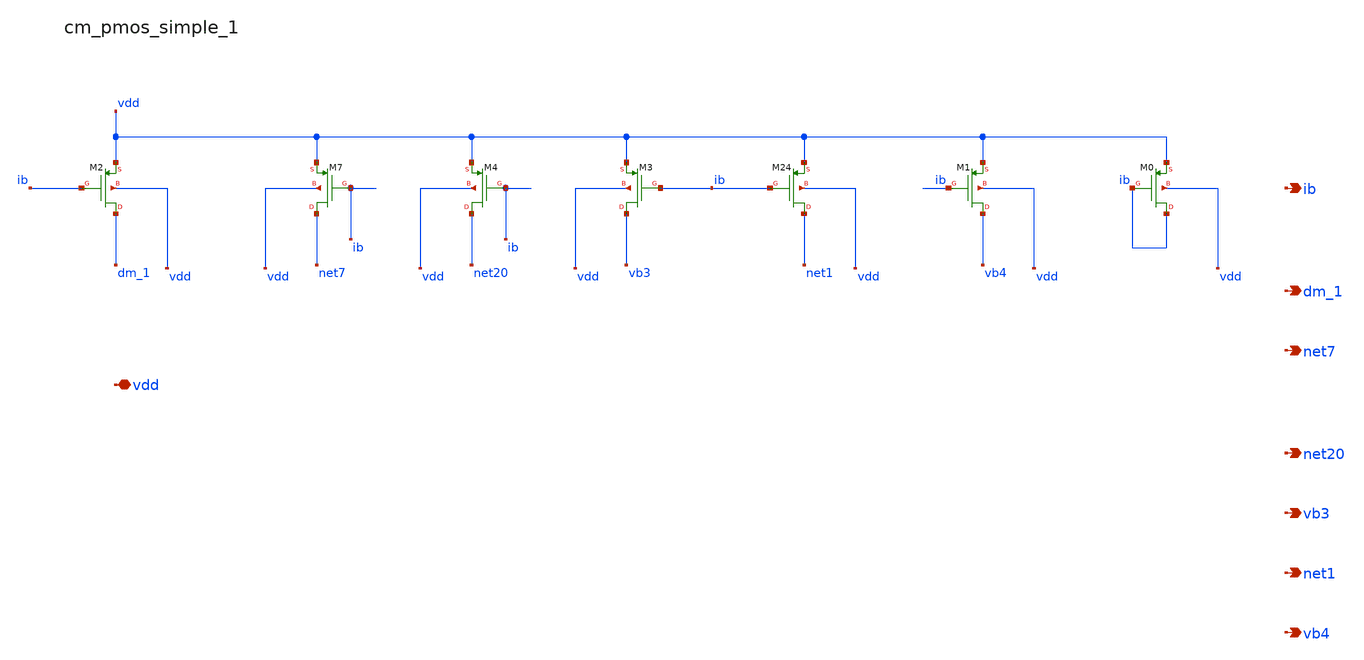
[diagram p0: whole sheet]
** sch_path: analog-db/raw/ldo_001_analoggym_basic/hier/blocks/cm_pmos_simple_1.sch
**.subckt cm_pmos_simple_1 vdd ib dm_1 net7 net20 vb3 net1 vb4
*.iopin vdd
*.opin ib
*.opin dm_1
*.opin net7
*.opin net20
*.opin vb3
*.opin net1
*.opin vb4
XM0 ib ib vdd vdd sg13_lv_pmos w=x_dut_xm0_w l=x_dut_xm0_l ng=1 m=x_dut_xm0_m
XM1 vb4 ib vdd vdd sg13_lv_pmos w=x_dut_xm1_w l=x_dut_xm1_l ng=1 m=x_dut_xm1_m
XM2 dm_1 ib vdd vdd sg13_lv_pmos w=x_dut_xm2_w l=x_dut_xm2_l ng=1 m=x_dut_xm2_m
XM24 net1 ib vdd vdd sg13_lv_pmos w=x_dut_xm24_w l=x_dut_xm24_l ng=1 m=x_dut_xm24_m
XM3 vb3 ib vdd vdd sg13_lv_pmos w=x_dut_xm3_w l=x_dut_xm3_l ng=1 m=x_dut_xm3_m
XM4 net20 ib vdd vdd sg13_lv_pmos w=x_dut_xm4_w l=x_dut_xm4_l ng=1 m=x_dut_xm4_m
XM7 net7 ib vdd vdd sg13_lv_pmos w=x_dut_xm7_w l=x_dut_xm7_l ng=1 m=x_dut_xm7_m
**.ends
.end
